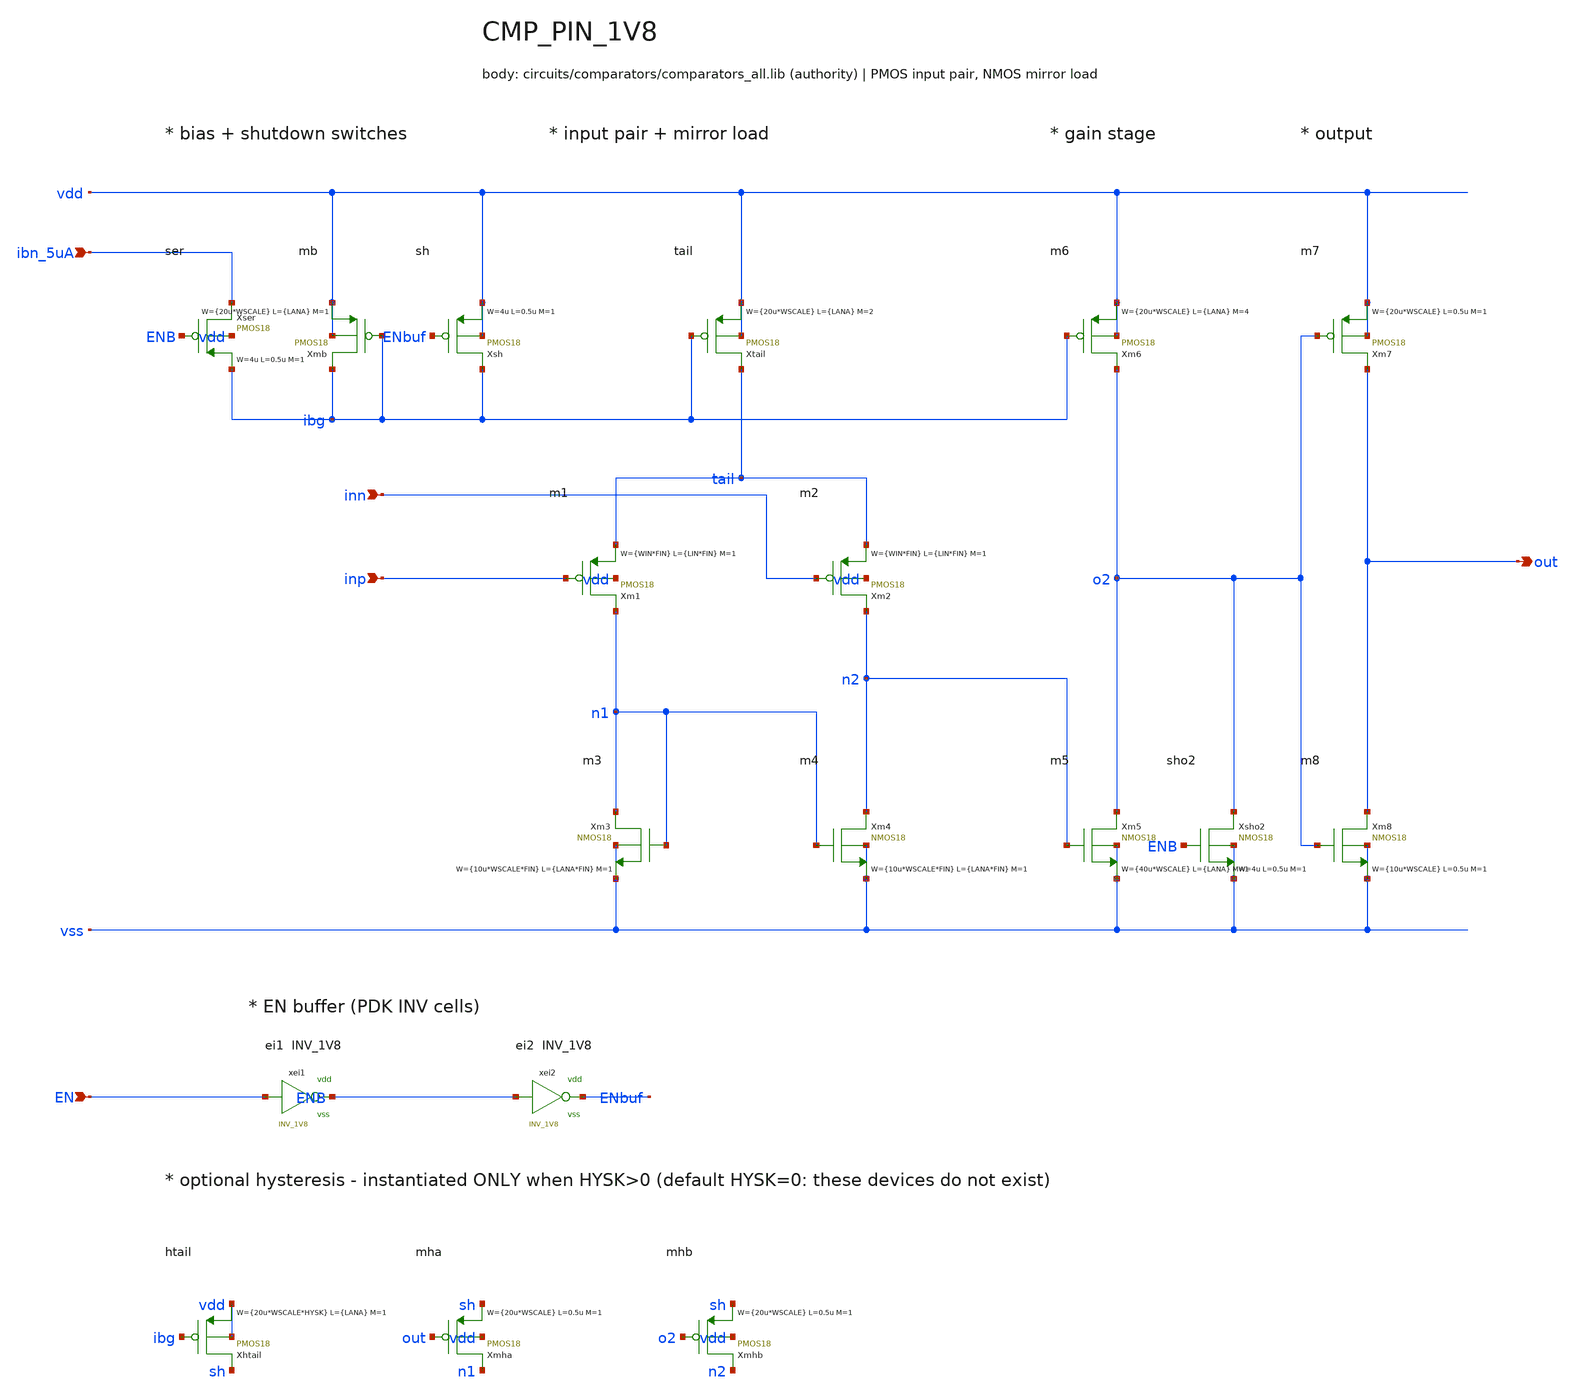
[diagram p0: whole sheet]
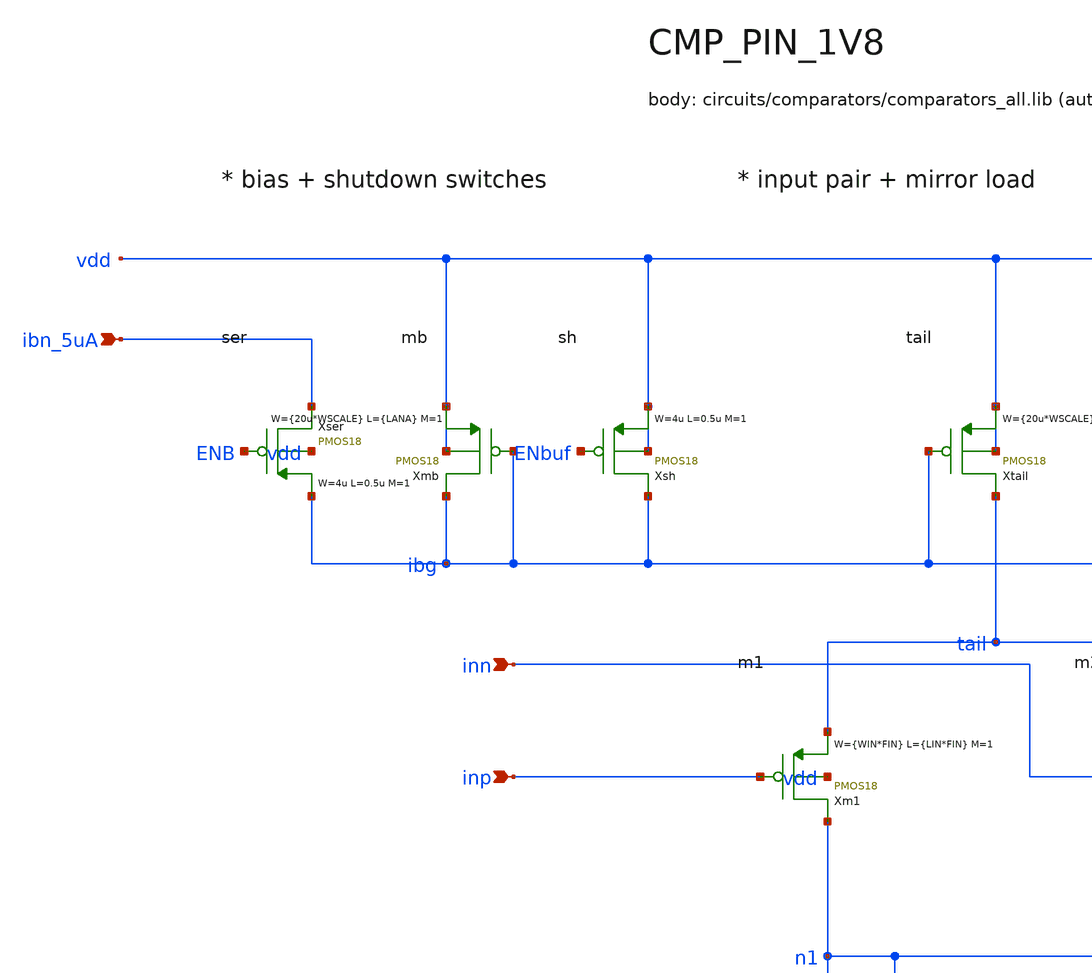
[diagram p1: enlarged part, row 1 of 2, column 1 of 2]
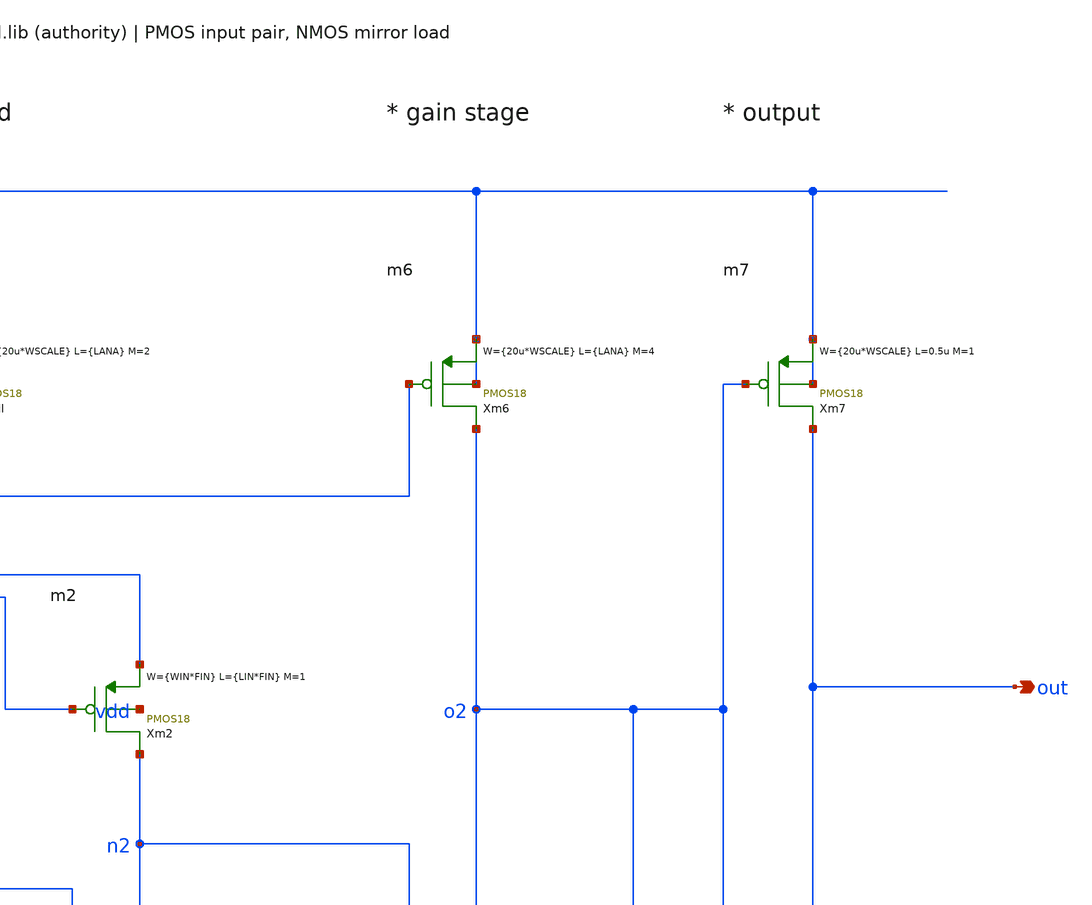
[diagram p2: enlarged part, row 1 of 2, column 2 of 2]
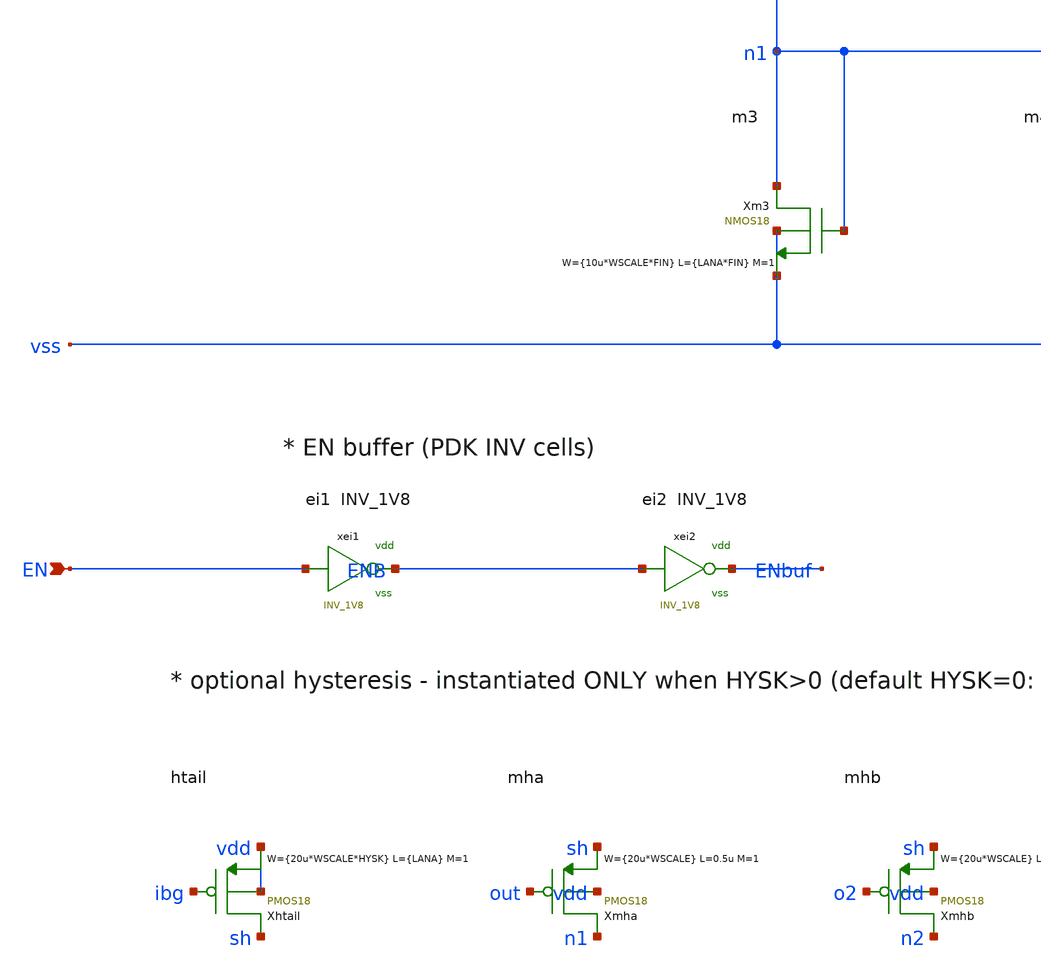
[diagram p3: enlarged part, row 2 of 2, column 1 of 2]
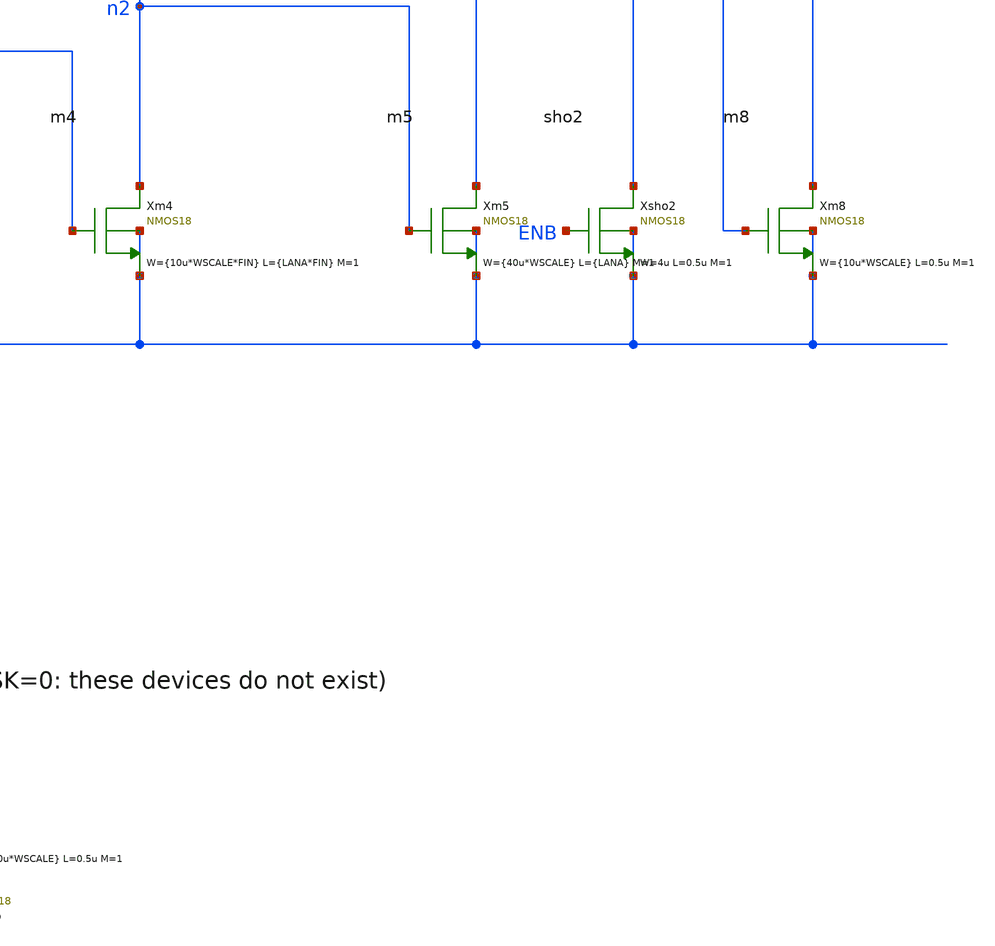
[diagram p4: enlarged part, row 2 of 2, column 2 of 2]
** sch_path: xschem/comparators/CMP_PIN_1V8.sch
**.subckt CMP_PIN_1V8 ibn_5uA out inp inn EN
*.ipin ibn_5uA
*.opin out
*.ipin inp
*.ipin inn
*.ipin EN
Xser ibn_5uA ENB ibg vdd PMOS18 W=4u L=0.5u M=1 MM_SIGMA=0
Xmb ibg ibg vdd vdd PMOS18 W={20u*WSCALE} L={LANA} M=1 MM_SIGMA=0
Xsh ibg ENbuf vdd vdd PMOS18 W=4u L=0.5u M=1 MM_SIGMA=0
Xtail tail ibg vdd vdd PMOS18 W={20u*WSCALE} L={LANA} M=2 MM_SIGMA=0
Xm1 n1 inp tail vdd PMOS18 W={WIN*FIN} L={LIN*FIN} M=1 MM_SIGMA=0
Xm2 n2 inn tail vdd PMOS18 W={WIN*FIN} L={LIN*FIN} M=1 MM_SIGMA=0
Xm3 n1 n1 vss vss NMOS18 W={10u*WSCALE*FIN} L={LANA*FIN} M=1 MM_SIGMA=0
Xm4 n2 n1 vss vss NMOS18 W={10u*WSCALE*FIN} L={LANA*FIN} M=1 MM_SIGMA=0
Xm5 o2 n2 vss vss NMOS18 W={40u*WSCALE} L={LANA} M=1 MM_SIGMA=0
Xm6 o2 ibg vdd vdd PMOS18 W={20u*WSCALE} L={LANA} M=4 MM_SIGMA=0
Xm7 out o2 vdd vdd PMOS18 W={20u*WSCALE} L=0.5u M=1 MM_SIGMA=0
Xm8 out o2 vss vss NMOS18 W={10u*WSCALE} L=0.5u M=1 MM_SIGMA=0
Xsho2 o2 ENB vss vss NMOS18 W=4u L=0.5u M=1 MM_SIGMA=0
xei1 EN ENB vdd vss INV_1V8
xei2 ENB ENbuf vdd vss INV_1V8
Xhtail sh ibg vdd vdd PMOS18 W={20u*WSCALE*HYSK} L={LANA} M=1 MM_SIGMA=0
Xmha n1 out sh vdd PMOS18 W={20u*WSCALE} L=0.5u M=1 MM_SIGMA=0
Xmhb n2 o2 sh vdd PMOS18 W={20u*WSCALE} L=0.5u M=1 MM_SIGMA=0
**.ends
.end
